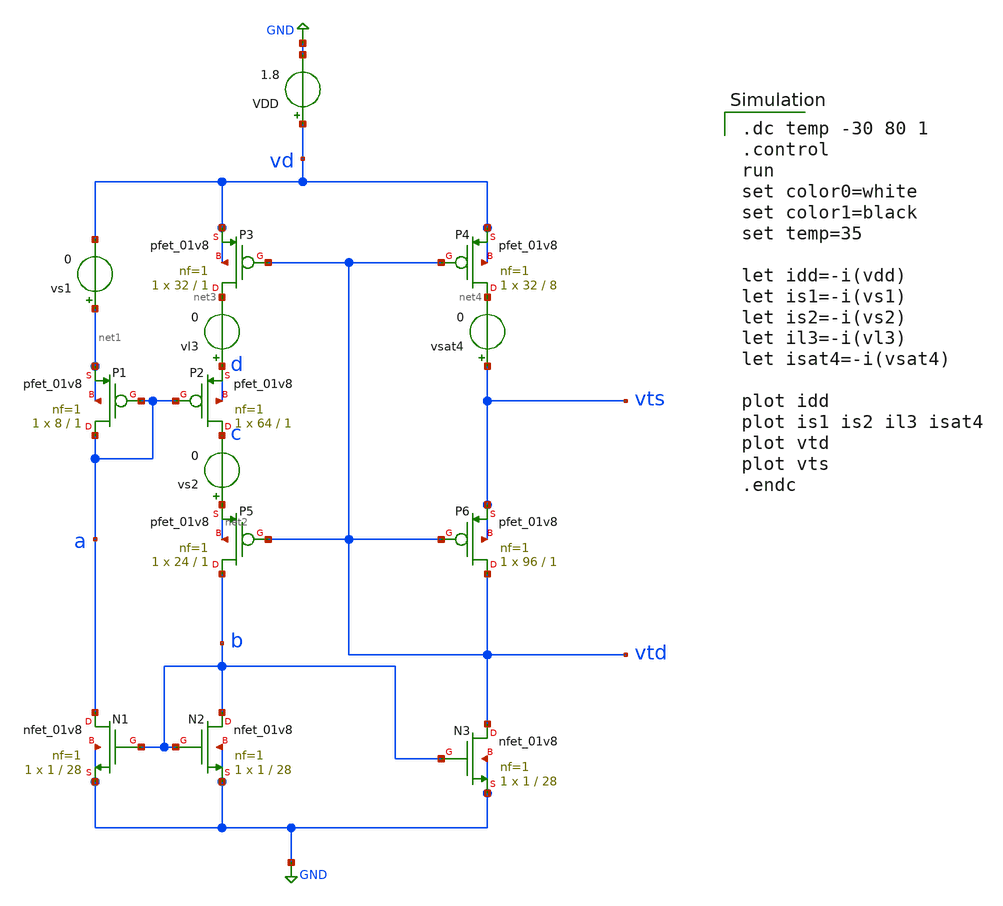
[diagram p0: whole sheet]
** sch_path: sensor/xschem/temp-tb-full.sch
**.subckt temp-tb-full
VDD vd GND 1.8
XP6 vtd vtd vts vts sky130_fd_pr__pfet_01v8 L=1 W=96 nf=1 ad='int((nf+1)/2) * W/nf * 0.29' as='int((nf+2)/2) * W/nf * 0.29'
+ pd='2*int((nf+1)/2) * (W/nf + 0.29)' ps='2*int((nf+2)/2) * (W/nf + 0.29)' nrd='0.29 / W' nrs='0.29 / W'
+ sa=0 sb=0 sd=0 mult=1 m=1
XN1 a b GND GND sky130_fd_pr__nfet_01v8 L=28 W=1 nf=1 ad='int((nf+1)/2) * W/nf * 0.29' as='int((nf+2)/2) * W/nf * 0.29'
+ pd='2*int((nf+1)/2) * (W/nf + 0.29)' ps='2*int((nf+2)/2) * (W/nf + 0.29)' nrd='0.29 / W' nrs='0.29 / W'
+ sa=0 sb=0 sd=0 mult=1 m=1
XP3 net3 vtd vd vd sky130_fd_pr__pfet_01v8 L=1 W=32 nf=1 ad='int((nf+1)/2) * W/nf * 0.29' as='int((nf+2)/2) * W/nf * 0.29'
+ pd='2*int((nf+1)/2) * (W/nf + 0.29)' ps='2*int((nf+2)/2) * (W/nf + 0.29)' nrd='0.29 / W' nrs='0.29 / W'
+ sa=0 sb=0 sd=0 mult=1 m=1
XP1 a a net1 net1 sky130_fd_pr__pfet_01v8 L=1 W=8 nf=1 ad='int((nf+1)/2) * W/nf * 0.29' as='int((nf+2)/2) * W/nf * 0.29'
+ pd='2*int((nf+1)/2) * (W/nf + 0.29)' ps='2*int((nf+2)/2) * (W/nf + 0.29)' nrd='0.29 / W' nrs='0.29 / W'
+ sa=0 sb=0 sd=0 mult=1 m=1
XP2 c a d d sky130_fd_pr__pfet_01v8 L=1 W=64 nf=1 ad='int((nf+1)/2) * W/nf * 0.29' as='int((nf+2)/2) * W/nf * 0.29'
+ pd='2*int((nf+1)/2) * (W/nf + 0.29)' ps='2*int((nf+2)/2) * (W/nf + 0.29)' nrd='0.29 / W' nrs='0.29 / W'
+ sa=0 sb=0 sd=0 mult=1 m=1
XP4 net4 vtd vd vd sky130_fd_pr__pfet_01v8 L=8 W=32 nf=1 ad='int((nf+1)/2) * W/nf * 0.29' as='int((nf+2)/2) * W/nf * 0.29'
+ pd='2*int((nf+1)/2) * (W/nf + 0.29)' ps='2*int((nf+2)/2) * (W/nf + 0.29)' nrd='0.29 / W' nrs='0.29 / W'
+ sa=0 sb=0 sd=0 mult=1 m=1
XN2 b b GND GND sky130_fd_pr__nfet_01v8 L=28 W=1 nf=1 ad='int((nf+1)/2) * W/nf * 0.29' as='int((nf+2)/2) * W/nf * 0.29'
+ pd='2*int((nf+1)/2) * (W/nf + 0.29)' ps='2*int((nf+2)/2) * (W/nf + 0.29)' nrd='0.29 / W' nrs='0.29 / W'
+ sa=0 sb=0 sd=0 mult=1 m=1
XN3 vtd b GND GND sky130_fd_pr__nfet_01v8 L=28 W=1 nf=1 ad='int((nf+1)/2) * W/nf * 0.29' as='int((nf+2)/2) * W/nf * 0.29'
+ pd='2*int((nf+1)/2) * (W/nf + 0.29)' ps='2*int((nf+2)/2) * (W/nf + 0.29)' nrd='0.29 / W' nrs='0.29 / W'
+ sa=0 sb=0 sd=0 mult=1 m=1
vs1 net1 vd 0
vs2 net2 c 0
vl3 d net3 0
vsat4 vts net4 0
XP5 b vtd net2 net2 sky130_fd_pr__pfet_01v8 L=1 W=24 nf=1 ad='int((nf+1)/2) * W/nf * 0.29' as='int((nf+2)/2) * W/nf * 0.29'
+ pd='2*int((nf+1)/2) * (W/nf + 0.29)' ps='2*int((nf+2)/2) * (W/nf + 0.29)' nrd='0.29 / W' nrs='0.29 / W'
+ sa=0 sb=0 sd=0 mult=1 m=1
**** begin user architecture code

.dc temp -30 80 1
.control
run
set color0=white
set color1=black
set temp=35

let idd=-i(vdd)
let is1=-i(vs1)
let is2=-i(vs2)
let il3=-i(vl3)
let isat4=-i(vsat4)

plot idd
plot is1 is2 il3 isat4
plot vtd
plot vts
.endc



.lib /home/hugodg/sky130_workspace/skywater-pdk/libraries/sky130_fd_pr_ngspice/latest/models/sky130.lib.spice tt

**** end user architecture code
**.ends
.GLOBAL GND
.end
